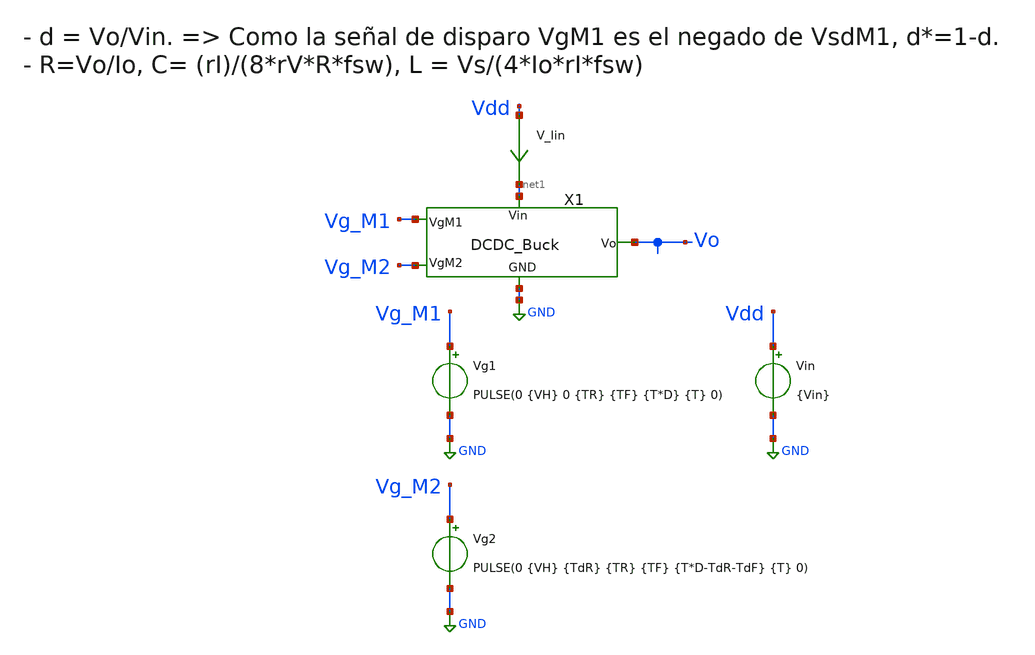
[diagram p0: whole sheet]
** sch_path: xschem/DCDCBuck/TB_DCDCBuck.sch
**.subckt TB_DCDCBuck
Vin Vdd GND {Vin}
Vg2 Vg_M2 GND PULSE(0 {VH} {TdR} {TR} {TF} {T*D-TdR-TdF} {T} 0)
Vg1 Vg_M1 GND PULSE(0 {VH} 0 {TR} {TF} {T*D} {T} 0)
V_Iin Vdd net1 0
.save i(v_iin)
X1 Vg_M1 Vg_M2 GND net1 Vo DCDC_Buck
**** begin user architecture code


.param Vin = 3.3
.param VH = 3.3
.param Del = 0

.ic v(Vo) = 0
*.ic i(x1.L1) = 0
*.ic v(Vc) = 0

*.param fsw = 15Meg
*.param fsw = 10Meg
*.param fsw = 8.4Meg
.param fsw = 5Meg
*.param fsw = 4.5Meg
*.param fsw = 1Meg

.param Vo = 1.2
.param Io = 1
.param rI = 0.3
.param rV = 0.1
.param T = 1/fsw

.param D = 1-((Vo+0.06)/(Vin-0.03))
*.param D = 1-((Vo)/(Vin-0.1))
.param TR = 0.01*T
.param TF = 0.01*T
.param TdR = 1n
.param TdF = 1n

*Filtro
.param L = Vin/(4*Io*rI*fsw)
.param R = Vo/Io
.param C = rI/(8*rV*R*fsw)

*.option temp = 125
*.option temp = -40
.option temp = 27





.save v(Vo) i(v.x1.V_Io) i(V_Iin) v(Vdd) v(x1.Vc) i(v.x1.V_IM2) i(v.x1.V_IL) v(Vg_M1) v(Vg_M2)
.param tau = 4*L/R
.csparam tau = {tau}
.param SimTime = tau+30*T
.csparam Sim_end = {SimTime}

.csparam T = {T}
.csparam L = {L}
.csparam C = {C}
.csparam R = {R}

.tran 1n {SimTime} uic

.control

run
set color0 = white
*tran 10n {SimTime} uic
*tran 10n {SimTime}

let Tmeas_i = {Sim_end} -{T}*10
let Tmeas_end = {Sim_end}

let Io = i(v.x1.V_Io)
*let Id_M1 = @m.x1.xm1.msky130_fd_pr__pfet_01v8[id]
let Id_M1 = i(V_Iin)
*let Id_M2 = @m.x1.xm2.msky130_fd_pr__nfet_01v8[id]
let Id_M2 = -i(v.x1.V_IM2)
let gds_M1 = @m.x1.xm1.msky130_fd_pr__pfet_01v8[gds]
let gds_M2 = @m.x1.xm2.msky130_fd_pr__nfet_01v8[gds]

let Po = Io*v(Vo)
let I_in = i(V_Iin)
let Pin = I_in*v(Vdd)
let Vsd_M1 = v(Vdd) - v(x1.Vc)
let Vds_M2 = v(x1.Vc)
let P_M1 = Vsd_M1*Id_M1
let P_M2 = -Vds_M2*Id_M2
let Ron_M1 = Vsd_M1/Id_M1
let Ron_M2 = Vds_M2/Id_M2
*let Ron_M1 = 1/gds_M1
*let Ron_M2 = 1/gds_M2

meas tran Vo_mean AVG v(Vo) FROM={Tmeas_i} TO={Tmeas_end}
meas tran Io_mean AVG Io FROM={Tmeas_i} TO={Tmeas_end}
meas tran Irms_M1 RMS Id_M1 FROM={Tmeas_i} TO={Tmeas_end}
meas tran Irms_M2 RMS Id_M2 FROM={Tmeas_i} TO={Tmeas_end}
meas tran Po_mean AVG Po FROM={Tmeas_i} TO={Tmeas_end}
meas tran Pin_mean AVG Pin FROM={Tmeas_i} TO={Tmeas_end}
meas tran P_M1_mean AVG P_M1 FROM={Tmeas_i} TO={Tmeas_end}
meas tran P_M2_mean AVG P_M2 FROM={Tmeas_i} TO={Tmeas_end}

let eff = 100*Po_mean/Pin_mean
let loss_M1 = 100*P_M1_mean/Pin_mean
let loss_M2 = 100*P_M2_mean/Pin_mean
let cond_loss_M1 = Irms_M1*Irms_M1*40m*100
let cond_loss_M2 = Irms_M2*Irms_M2*35m*100
let sumaPot = eff+loss_M1+loss_M2
print eff loss_M1 loss_M2 cond_loss_M1 cond_loss_M2 sumaPot
print tau T L C R

plot Io i(v.x1.V_IL)
plot Id_M1 Id_M2
plot v(Vo)
plot Po Pin
*plot P_M1 P_M2
plot v(x1.Vc)
plot v(Vg_M1) v(Vg_M2)
plot Ron_M1 Ron_M2
*plot i(V_Iload)
write TB_DCDCBuck.raw
.endc


.end




.lib cornerMOShv.lib mos_tt
.lib cornerMOSlv.lib mos_tt
*.lib cornerMOShv.lib mos_ff
*.lib cornerMOSlv.lib mos_ff
*.lib cornerMOShv.lib mos_ss
*.lib cornerMOSlv.lib mos_ss
*.lib cornerMOShv.lib mos_sf
*.lib cornerMOSlv.lib mos_sf
*.lib cornerMOShv.lib mos_fs
*.lib cornerMOSlv.lib mos_fs

.include /opt/pdks/ihp-sg13g2/libs.ref/sg13g2_stdcell/spice/sg13g2_stdcell.spice
.lib $::SG13G2_MODELS/cornerRES.lib res_typ
.lib $::SG13G2_MODELS/cornerCAP.lib cap_typ
*.lib $::SG13G2_MODELS/diodes.lib



.param mult = 95238
.param temp=27
.param mult_M1 = 3*mult
.param w_M1 =0.3u
.param l_M1 = 0.45u
.param ng_M1 = 1

.param mult_M2 = 1*mult
.param w_M2 =0.3u
.param l_M2 =0.45u
.param ng_M2 =1








**** end user architecture code
**.ends

* expanding   symbol:  ../DCDCBuck/DCDC_Buck.sym # of pins=5
** sym_path: xschem/DCDCBuck/DCDC_Buck.sym
** sch_path: xschem/DCDCBuck/DCDC_Buck.sch
.subckt DCDC_Buck VgM1 VgM2 GND Vin Vo
*.iopin Vin
*.ipin VgM1
*.ipin VgM2
*.iopin Vo
*.iopin GND
L1 net2 net1 {L} m=1
C1 net1 GND {C} m=1
V_Io net1 Vo 0
.save i(v_io)
V_IL Vc net2 0
.save i(v_il)
R1 Vo GND {R} m=1
V_IM2 Vc net3 0
.save i(v_im2)
XM3 Vc VgM1 Vin Vin sg13_hv_pmos w={w_M1} l={l_M1} ng={ng_M1} m={mult_M1} mm_ok=1
XM1 GND VgM2 net3 GND sg13_hv_nmos w={w_M2} l={l_M2} ng={ng_M2} m={mult_M2} mm_ok=1
.ends

.GLOBAL GND
.end
